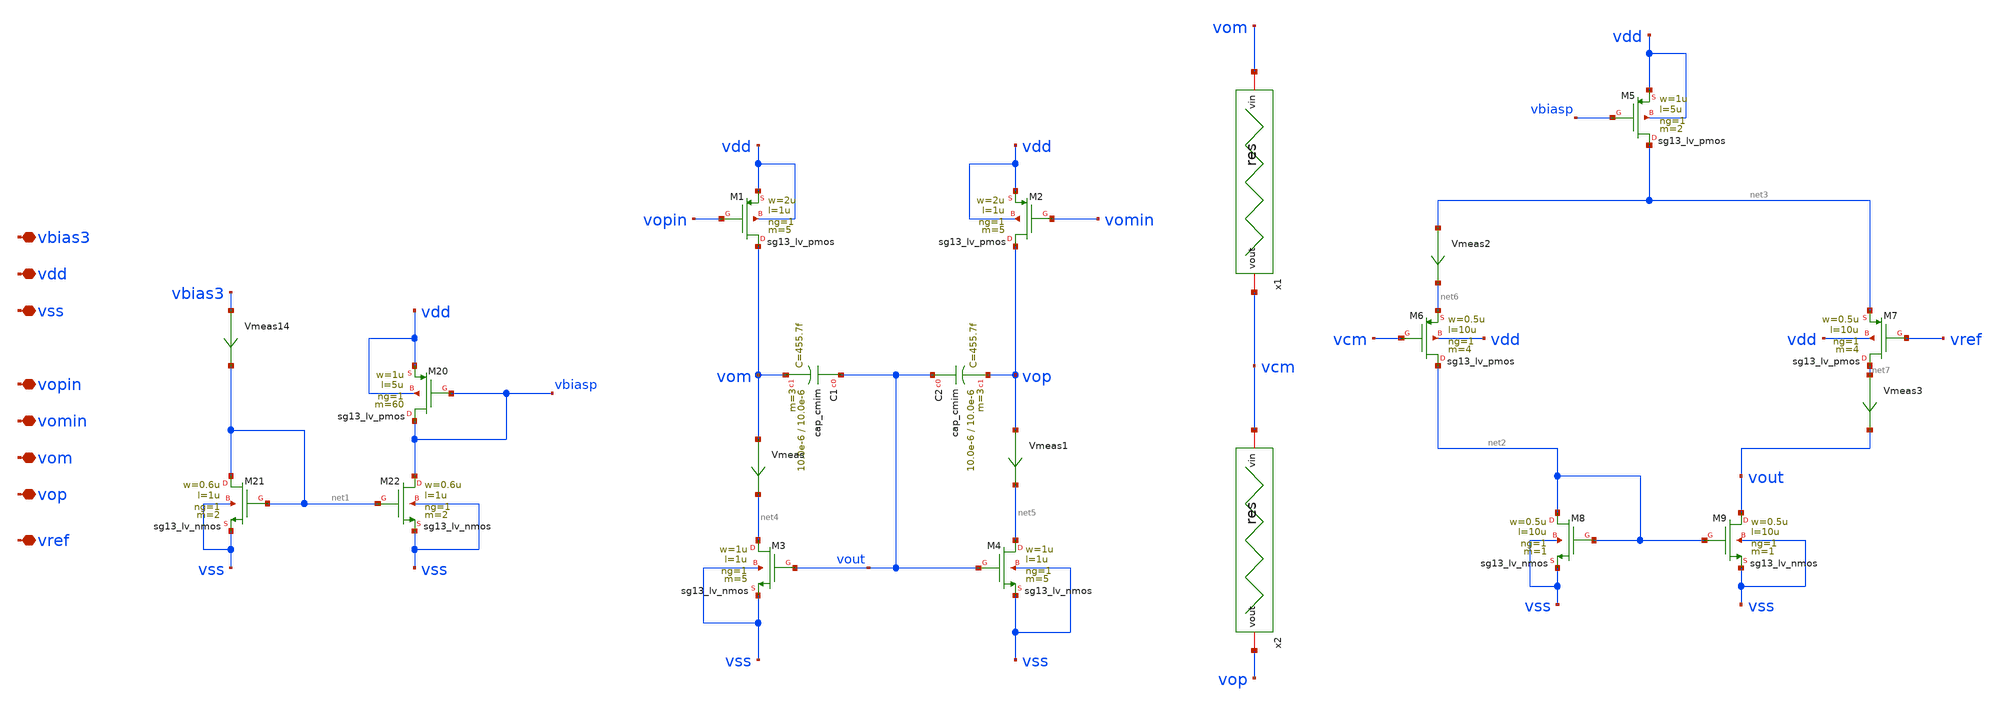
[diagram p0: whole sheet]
** sch_path: src/Opamp_Design/src/Common_source_stage.sch
**.subckt Common_source_stage vbias3 vdd vss vopin vomin vom vop vref
*.iopin vbias3
*.iopin vdd
*.iopin vss
*.iopin vopin
*.iopin vomin
*.iopin vom
*.iopin vop
*.iopin vref
XM20 vbiasp vbiasp vdd vdd sg13_lv_pmos w=1u l=5u ng=1 m=60 mm_ok=1
XM21 net1 net1 vss vss sg13_lv_nmos w=0.6u l=1u ng=1 m=2 mm_ok=1
XM22 vbiasp net1 vss vss sg13_lv_nmos w=0.6u l=1u ng=1 m=2 mm_ok=1
Vmeas14 vbias3 net1 0
.save i(vmeas14)
XM1 vom vopin vdd vdd sg13_lv_pmos w=2u l=1u ng=1 m=5 mm_ok=1
XM2 vop vomin vdd vdd sg13_lv_pmos w=2u l=1u ng=1 m=5 mm_ok=1
XM3 net4 vout vss vss sg13_lv_nmos w=1u l=1u ng=1 m=5 mm_ok=1
XM4 net5 vout vss vss sg13_lv_nmos w=1u l=1u ng=1 m=5 mm_ok=1
XM5 net3 vbiasp vdd vdd sg13_lv_pmos w=1u l=5u ng=1 m=2 mm_ok=1
XM6 net2 vcm net6 vdd sg13_lv_pmos w=0.5u l=10u ng=1 m=4 mm_ok=1
XM7 net7 vref net3 vdd sg13_lv_pmos w=0.5u l=10u ng=1 m=4 mm_ok=1
XM8 net2 net2 vss vss sg13_lv_nmos w=0.5u l=10u ng=1 m=1 mm_ok=1
XM9 vout net2 vss vss sg13_lv_nmos w=0.5u l=10u ng=1 m=1 mm_ok=1
XC1 vout vom cap_cmim w=10.0e-6 l=10.0e-6 m=3 mm_ok=1
XC2 vout vop cap_cmim w=10.0e-6 l=10.0e-6 m=3 mm_ok=1
x1 vom vcm res
x2 vcm vop res
Vmeas vom net4 0
.save i(vmeas)
Vmeas1 vop net5 0
.save i(vmeas1)
Vmeas2 net3 net6 0
.save i(vmeas2)
Vmeas3 net7 vout 0
.save i(vmeas3)
**.ends
.end
